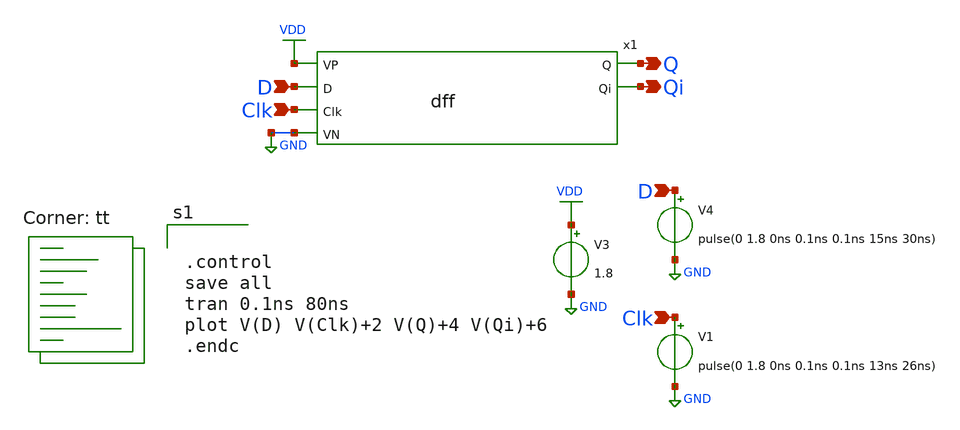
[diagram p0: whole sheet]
** sch_path: dff/xschem/tb_xschem_dff.sch
**.subckt tb_xschem_dff D Clk D Clk Qi Q
*.ipin D
*.ipin Clk
*.ipin D
*.ipin Clk
*.opin Qi
*.opin Q
V3 VDD GND 1.8
V4 D GND pulse(0 1.8 0ns 0.1ns 0.1ns 15ns 30ns)
V1 Clk GND pulse(0 1.8 0ns 0.1ns 0.1ns 13ns 26ns)
x1 Q VDD D Clk GND Qi dff
**** begin user architecture code
.lib $::SKYWATER_MODELS/sky130.lib.spice tt


.control
save all
tran 0.1ns 80ns
plot V(D) V(Clk)+2 V(Q)+4 V(Qi)+6
.endc


**** end user architecture code
**.ends

* expanding   symbol:  dff.sym # of pins=6
** sym_path: dff/xschem/dff.sym
** sch_path: dff/xschem/dff.sch
.subckt dff Q VP D Clk VN Qi
*.ipin D
*.ipin Clk
*.ipin VP
*.ipin VN
*.opin Q
*.opin Qi
x1 VP D net1 VN inverter
x2 VP net2 Clk D VN nand
x3 VP net3 Clk net1 VN nand
x4 VP Qi net3 Q VN nand
x5 VP Q Qi net2 VN nand
.ends


* expanding   symbol:  /foss/designs/APIC_Mux_DFF/basic_cell/single_cell/inverter/inverter.sym # of
*+ pins=4
** sym_path: basic_cell/single_cell/inverter/inverter.sym
** sch_path: basic_cell/single_cell/inverter/inverter.sch
.subckt inverter VP A OUT VN
*.ipin A
*.ipin VP
*.ipin VN
*.opin OUT
XM1 OUT A VP VP sky130_fd_pr__pfet_01v8 L=0.15 W=3 nf=1 ad='int((nf+1)/2) * W/nf * 0.29' as='int((nf+2)/2) * W/nf * 0.29'
+ pd='2*int((nf+1)/2) * (W/nf + 0.29)' ps='2*int((nf+2)/2) * (W/nf + 0.29)' nrd='0.29 / W' nrs='0.29 / W'
+ sa=0 sb=0 sd=0 mult=1 m=1
XM2 OUT A VN VN sky130_fd_pr__nfet_01v8 L=0.15 W=1 nf=1 ad='int((nf+1)/2) * W/nf * 0.29' as='int((nf+2)/2) * W/nf * 0.29'
+ pd='2*int((nf+1)/2) * (W/nf + 0.29)' ps='2*int((nf+2)/2) * (W/nf + 0.29)' nrd='0.29 / W' nrs='0.29 / W'
+ sa=0 sb=0 sd=0 mult=1 m=1
.ends


* expanding   symbol:  /foss/designs/APIC_Mux_DFF/basic_cell/single_cell/nand/nand.sym # of pins=5
** sym_path: basic_cell/single_cell/nand/nand.sym
** sch_path: basic_cell/single_cell/nand/nand.sch
.subckt nand VP OUT B A VN
*.opin OUT
*.ipin A
*.ipin B
*.ipin VN
*.ipin VP
XM4 OUT A net1 VN sky130_fd_pr__nfet_01v8 L=0.15 W=1 nf=1 ad='int((nf+1)/2) * W/nf * 0.29' as='int((nf+2)/2) * W/nf * 0.29'
+ pd='2*int((nf+1)/2) * (W/nf + 0.29)' ps='2*int((nf+2)/2) * (W/nf + 0.29)' nrd='0.29 / W' nrs='0.29 / W'
+ sa=0 sb=0 sd=0 mult=1 m=1
XM3 net1 B VN VN sky130_fd_pr__nfet_01v8 L=0.15 W=1 nf=1 ad='int((nf+1)/2) * W/nf * 0.29' as='int((nf+2)/2) * W/nf * 0.29'
+ pd='2*int((nf+1)/2) * (W/nf + 0.29)' ps='2*int((nf+2)/2) * (W/nf + 0.29)' nrd='0.29 / W' nrs='0.29 / W'
+ sa=0 sb=0 sd=0 mult=1 m=1
XM1 OUT A VP VP sky130_fd_pr__pfet_01v8 L=0.15 W=3 nf=1 ad='int((nf+1)/2) * W/nf * 0.29' as='int((nf+2)/2) * W/nf * 0.29'
+ pd='2*int((nf+1)/2) * (W/nf + 0.29)' ps='2*int((nf+2)/2) * (W/nf + 0.29)' nrd='0.29 / W' nrs='0.29 / W'
+ sa=0 sb=0 sd=0 mult=1 m=1
XM2 OUT B VP VP sky130_fd_pr__pfet_01v8 L=0.15 W=3 nf=1 ad='int((nf+1)/2) * W/nf * 0.29' as='int((nf+2)/2) * W/nf * 0.29'
+ pd='2*int((nf+1)/2) * (W/nf + 0.29)' ps='2*int((nf+2)/2) * (W/nf + 0.29)' nrd='0.29 / W' nrs='0.29 / W'
+ sa=0 sb=0 sd=0 mult=1 m=1
.ends

.GLOBAL VDD
.GLOBAL GND
.end
